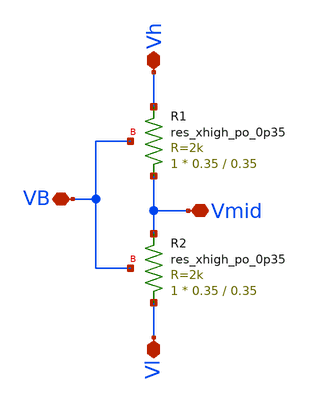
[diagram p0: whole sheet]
** sch_path: Circuits/Primitives/RString/RString.sch
**.subckt RString Vh VB Vmid Vl
*.iopin Vh
*.iopin VB
*.iopin Vmid
*.iopin Vl
XR1 Vmid Vh VB sky130_fd_pr__res_xhigh_po_0p35 L=0.35 mult=1 m=1
XR2 Vl Vmid VB sky130_fd_pr__res_xhigh_po_0p35 L=0.35 mult=1 m=1
**.ends
.end
